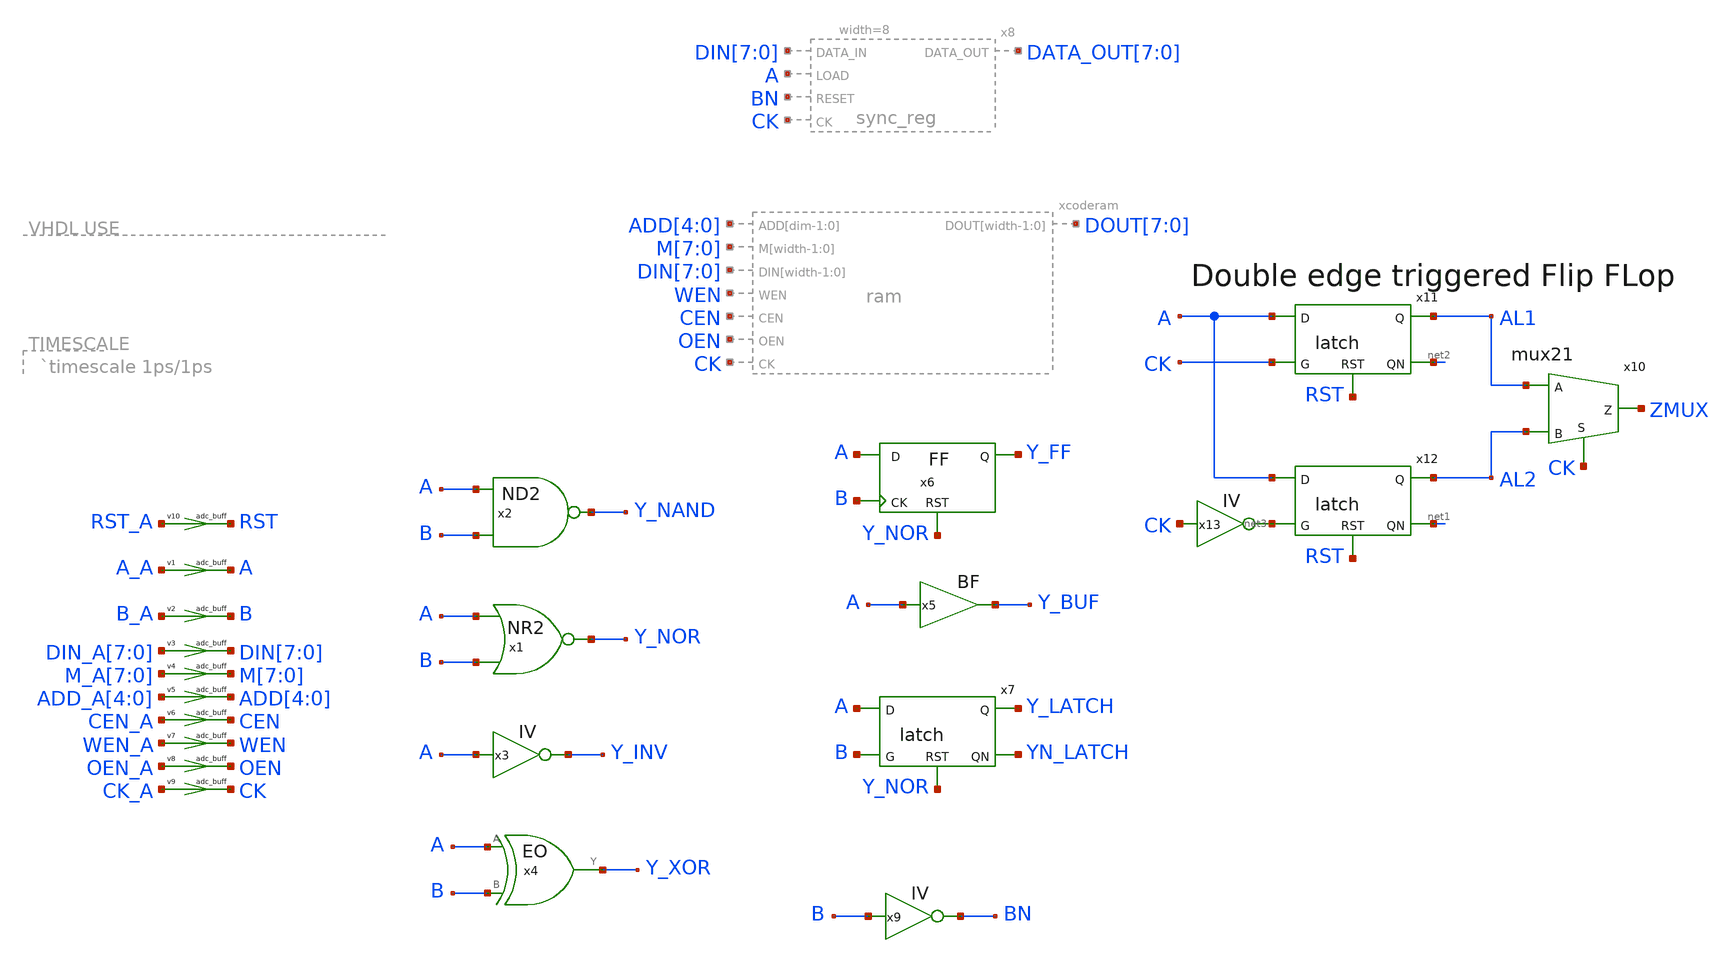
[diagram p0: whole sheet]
** sch_path: xschem-src/xschem_library/logic/testbench.sch
* Copyright (C) 1998-2026 Stefan Frederik Schippers
* This program is free software; you can redistribute it and/or modify
* it under the terms of the GNU General Public License as published by
* the Free Software Foundation; either version 2 of the License, or
* (at your option) any later version.
* This program is distributed in the hope that it will be useful,
* but WITHOUT ANY WARRANTY; without even the implied warranty of
* MERCHANTABILITY or FITNESS FOR A PARTICULAR PURPOSE.  See the
* GNU General Public License for more details.
* You should have received a copy of the GNU General Public License
* along with this program; if not, write to the Free Software
**.subckt testbench
x1 [ A B ] Y_NOR nor
x2 [ A B ] Y_NAND nand
x3 [ A ] Y_INV inv
x4 Y_XOR A B eo
x5 Y_BUF A bf
x6 A Y_FF B Y_NOR ff
x7 A Y_LATCH B Y_NOR YN_LATCH latch
x9 [ B ] BN inv
v1 [ A_A ] [ A ] adc_buff
v2 [ B_A ] [ B ] adc_buff
v3 [ DIN_A[7] ] [ DIN[7] ] adc_buff
v4 [ M_A[7] ] [ M[7] ] adc_buff
v5 [ ADD_A[4] ] [ ADD[4] ] adc_buff
v6 [ CEN_A ] [ CEN ] adc_buff
v7 [ WEN_A ] [ WEN ] adc_buff
v8 [ OEN_A ] [ OEN ] adc_buff
v9 [ CK_A ] [ CK ] adc_buff
x10 AL1 ZMUX AL2 CK mux21
x11 A AL1 CK RST net2 latch
x12 A AL2 net3 RST net1 latch
x13 [ CK ] net3 inv
v10 [ RST_A ] [ RST ] adc_buff
**.ends

* expanding   symbol:  eo.sym # of pins=3
** sym_path: xschem-src/xschem_library/logic/eo.sym
** sch_path: xschem-src/xschem_library/logic/eo.sch
.subckt eo Y A B  delay=220 ps del=220
*.ipin A
*.ipin B
*.opin Y
.ends


* expanding   symbol:  bf.sym # of pins=2
** sym_path: xschem-src/xschem_library/logic/bf.sym
** sch_path: xschem-src/xschem_library/logic/bf.sch
.subckt bf Y A  delay=90 ps del=90
*.opin Y
*.ipin A
.ends


* expanding   symbol:  ff.sym # of pins=4
** sym_path: xschem-src/xschem_library/logic/ff.sym
** sch_path: xschem-src/xschem_library/logic/ff.sch
.subckt ff D Q CK RST  delay=400 ps del=400
*.ipin D
*.opin Q
*.ipin CK
*.ipin RST
.ends


* expanding   symbol:  latch.sym # of pins=5
** sym_path: xschem-src/xschem_library/logic/latch.sym
** sch_path: xschem-src/xschem_library/logic/latch.sch
.subckt latch D Q G RST QN  delay=200 ps del=200
*.opin Q
*.ipin G
*.ipin RST
*.opin QN
*.ipin D
* noconn Q
* noconn QN
* noconn RST
* noconn D
* noconn G
.ends


* expanding   symbol:  ram.sym # of pins=8
** sym_path: xschem-src/xschem_library/logic/ram.sym
** sch_path: xschem-src/xschem_library/logic/ram.sch
.subckt ram CK OEN CEN WEN DIN[width-1:0] M[width-1:0] ADD[dim-1:0] DOUT[width-1:0]  dim=5 width=8
+ hex=0
datafile=ram.list modulename=ram access_delay=3000 oe_delay=300
*.opin DOUT[width-1:0]
*.ipin DIN[width-1:0]
*.ipin CK
*.ipin OEN
*.ipin ADD[dim-1:0]
*.ipin WEN
*.ipin CEN
*.ipin M[width-1:0]
.ends


* expanding   symbol:  sync_reg.sym # of pins=5
** sym_path: xschem-src/xschem_library/logic/sync_reg.sym
** sch_path: xschem-src/xschem_library/logic/sync_reg.sch
.subckt sync_reg DATA_OUT[width-1:0] CK RESET DATA_IN[width-1:0] LOAD  width=8 del=400 delay=400 ps
*.opin DATA_OUT[width-1:0]
*.ipin CK
*.ipin RESET
*.ipin DATA_IN[width-1:0]
*.ipin LOAD
.ends


* expanding   symbol:  mux21.sym # of pins=4
** sym_path: xschem-src/xschem_library/logic/mux21.sym
** sch_path: xschem-src/xschem_library/logic/mux21.sch
.subckt mux21 A Z B S  delay=200 ps del=200
*.opin Z
*.ipin S
*.ipin A
*.ipin B
* noconn Z
* noconn A
* noconn B
* noconn S
.ends

.end
